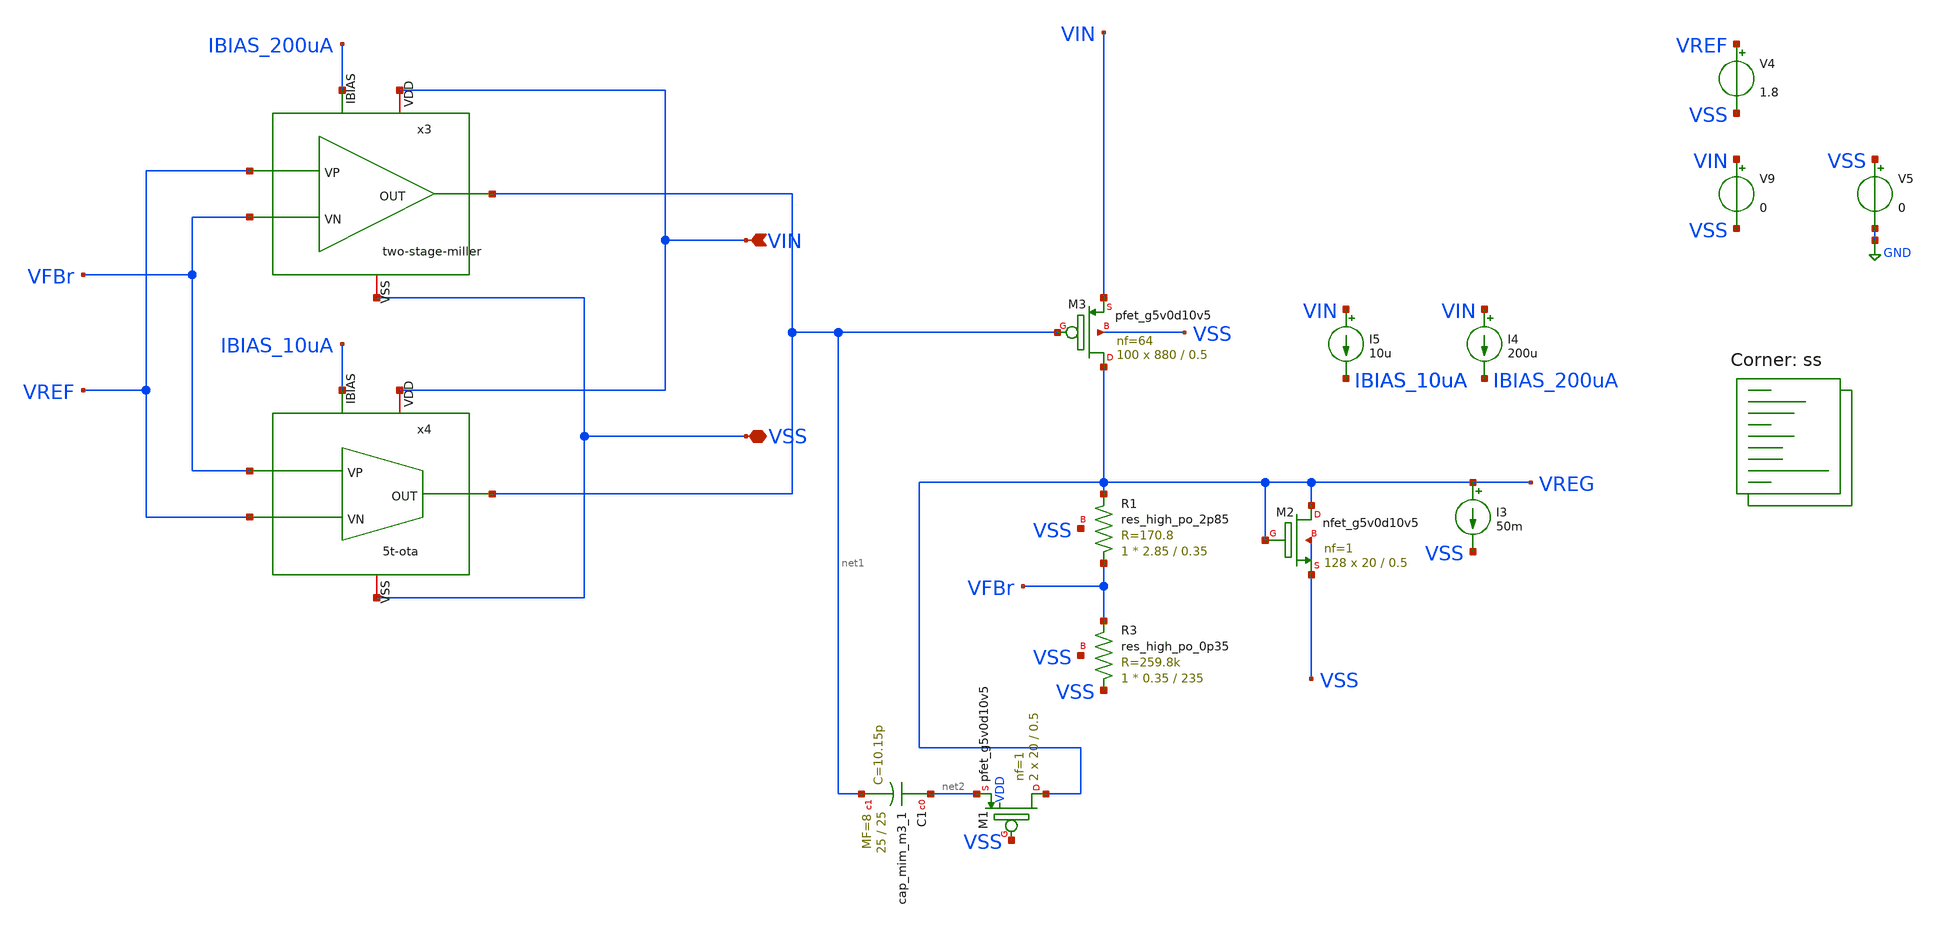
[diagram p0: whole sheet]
** sch_path: bandgap/testbench/tb_dc_dropout.sch
**.subckt tb_dc_dropout VIN VSS
*.ipin VIN
*.iopin VSS
XR3 VSS VFBr VSS sky130_fd_pr__res_high_po_0p35 L=235 mult=1 m=1
XR1 VFBr VREG VSS sky130_fd_pr__res_high_po_2p85 L=0.35 mult=1 m=1
x3 VIN net1 VREF VFBr IBIAS_200uA VSS two-stage-miller
x4 VIN net1 IBIAS_10uA VREF VFBr VSS 5t-ota
I4 VIN IBIAS_200uA 200u
I3 VREG VSS 50m
V4 VREF VSS 1.8
V5 VSS GND 0
V9 VIN VSS 0
I5 VIN IBIAS_10uA 10u
XM2 VREG VREG VSS VSS sky130_fd_pr__nfet_g5v0d10v5 L=0.5 W=20 nf=1 ad='int((nf+1)/2) * W/nf * 0.29' as='int((nf+2)/2) * W/nf * 0.29'
+ pd='2*int((nf+1)/2) * (W/nf + 0.29)' ps='2*int((nf+2)/2) * (W/nf + 0.29)' nrd='0.29 / W' nrs='0.29 / W'
+ sa=0 sb=0 sd=0 mult=128 m=128
XC1 net2 net1 sky130_fd_pr__cap_mim_m3_1 W=25 L=25 MF=8 m=8
XM1 VREG VSS net2 VDD sky130_fd_pr__pfet_g5v0d10v5 L=0.5 W=20 nf=1 ad='int((nf+1)/2) * W/nf * 0.29' as='int((nf+2)/2) * W/nf * 0.29'
+ pd='2*int((nf+1)/2) * (W/nf + 0.29)' ps='2*int((nf+2)/2) * (W/nf + 0.29)' nrd='0.29 / W' nrs='0.29 / W'
+ sa=0 sb=0 sd=0 mult=2 m=2
XM3 VREG net1 VIN VSS sky130_fd_pr__pfet_g5v0d10v5 L=0.5 W=880 nf=64 ad='int((nf+1)/2) * W/nf * 0.29'
+ as='int((nf+2)/2) * W/nf * 0.29' pd='2*int((nf+1)/2) * (W/nf + 0.29)' ps='2*int((nf+2)/2) * (W/nf + 0.29)'
+ nrd='0.29 / W' nrs='0.29 / W' sa=0 sb=0 sd=0 mult=100 m=100
**** begin user architecture code


.control
DC V9 0 5 0.01

* Nominal output voltage (from regulation region)
let Vout_nom = 0.5
let Vout_95  = 0.95*Vout_nom

* Find Vin where Vout crosses 95%
meas dc Vin_do find v(vin) when v(vreg)=Vout_95

* Measure Vout at that Vin (for completeness)
meas dc Vout_do find v(vreg) when v(vreg)=Vout_95

* Compute dropout voltage
let Vdo = Vin_do - Vout_do
print vdo
plot VIN VREG
.endc


.lib $::SKYWATER_MODELS/sky130.lib.spice ss
**** end user architecture code
**.ends

* expanding   symbol:  icdec-biomedical-pmic/xschem/error-amplifier/schematics/two-stage-miller.sym
*+ # of pins=6
** sym_path: xschem/error-amplifier/schematics/two-stage-miller.sym
** sch_path: xschem/error-amplifier/schematics/two-stage-miller.sch
.subckt two-stage-miller VDD OUT VP VN IBIAS VSS
*.iopin VDD
*.iopin VSS
*.ipin IBIAS
*.ipin VP
*.ipin VN
*.opin OUT
XM1 net3 net2 VDD VDD sky130_fd_pr__pfet_g5v0d10v5 L=1.25 W=75.2 nf=8 ad='int((nf+1)/2) * W/nf * 0.29'
+ as='int((nf+2)/2) * W/nf * 0.29' pd='2*int((nf+1)/2) * (W/nf + 0.29)' ps='2*int((nf+2)/2) * (W/nf + 0.29)'
+ nrd='0.29 / W' nrs='0.29 / W' sa=0 sb=0 sd=0 mult=1 m=1
XM2 net2 net2 VDD VDD sky130_fd_pr__pfet_g5v0d10v5 L=1.25 W=75.2 nf=8 ad='int((nf+1)/2) * W/nf * 0.29'
+ as='int((nf+2)/2) * W/nf * 0.29' pd='2*int((nf+1)/2) * (W/nf + 0.29)' ps='2*int((nf+2)/2) * (W/nf + 0.29)'
+ nrd='0.29 / W' nrs='0.29 / W' sa=0 sb=0 sd=0 mult=1 m=1
XM3 net3 VN net1 VSS sky130_fd_pr__nfet_g5v0d10v5 L=0.5 W=37.7 nf=8 ad='int((nf+1)/2) * W/nf * 0.29'
+ as='int((nf+2)/2) * W/nf * 0.29' pd='2*int((nf+1)/2) * (W/nf + 0.29)' ps='2*int((nf+2)/2) * (W/nf + 0.29)'
+ nrd='0.29 / W' nrs='0.29 / W' sa=0 sb=0 sd=0 mult=1 m=1
XM4 net2 VP net1 VSS sky130_fd_pr__nfet_g5v0d10v5 L=0.5 W=37.7 nf=8 ad='int((nf+1)/2) * W/nf * 0.29'
+ as='int((nf+2)/2) * W/nf * 0.29' pd='2*int((nf+1)/2) * (W/nf + 0.29)' ps='2*int((nf+2)/2) * (W/nf + 0.29)'
+ nrd='0.29 / W' nrs='0.29 / W' sa=0 sb=0 sd=0 mult=1 m=1
XM5 net1 IBIAS VSS VSS sky130_fd_pr__nfet_g5v0d10v5 L=1.25 W=60 nf=8 ad='int((nf+1)/2) * W/nf * 0.29'
+ as='int((nf+2)/2) * W/nf * 0.29' pd='2*int((nf+1)/2) * (W/nf + 0.29)' ps='2*int((nf+2)/2) * (W/nf + 0.29)'
+ nrd='0.29 / W' nrs='0.29 / W' sa=0 sb=0 sd=0 mult=1 m=1
XM6 IBIAS IBIAS VSS VSS sky130_fd_pr__nfet_g5v0d10v5 L=1.25 W=60 nf=8 ad='int((nf+1)/2) * W/nf * 0.29'
+ as='int((nf+2)/2) * W/nf * 0.29' pd='2*int((nf+1)/2) * (W/nf + 0.29)' ps='2*int((nf+2)/2) * (W/nf + 0.29)'
+ nrd='0.29 / W' nrs='0.29 / W' sa=0 sb=0 sd=0 mult=1 m=1
XM7 OUT net3 VDD VDD sky130_fd_pr__pfet_g5v0d10v5 L=1.25 W=160 nf=16 ad='int((nf+1)/2) * W/nf * 0.29'
+ as='int((nf+2)/2) * W/nf * 0.29' pd='2*int((nf+1)/2) * (W/nf + 0.29)' ps='2*int((nf+2)/2) * (W/nf + 0.29)'
+ nrd='0.29 / W' nrs='0.29 / W' sa=0 sb=0 sd=0 mult=1 m=1
XM8 OUT IBIAS VSS VSS sky130_fd_pr__nfet_g5v0d10v5 L=1.25 W=60 nf=8 ad='int((nf+1)/2) * W/nf * 0.29'
+ as='int((nf+2)/2) * W/nf * 0.29' pd='2*int((nf+1)/2) * (W/nf + 0.29)' ps='2*int((nf+2)/2) * (W/nf + 0.29)'
+ nrd='0.29 / W' nrs='0.29 / W' sa=0 sb=0 sd=0 mult=1 m=1
XC1 net4 net3 sky130_fd_pr__cap_mim_m3_1 W=25 L=25 MF=8 m=8
XM9 OUT VSS net4 VDD sky130_fd_pr__pfet_g5v0d10v5 L=0.9 W=20 nf=4 ad='int((nf+1)/2) * W/nf * 0.29' as='int((nf+2)/2) * W/nf * 0.29'
+ pd='2*int((nf+1)/2) * (W/nf + 0.29)' ps='2*int((nf+2)/2) * (W/nf + 0.29)' nrd='0.29 / W' nrs='0.29 / W'
+ sa=0 sb=0 sd=0 mult=1 m=1
.ends


* expanding   symbol:  icdec-biomedical-pmic/xschem/5t-ota/schematics/5t-ota.sym # of pins=6
** sym_path: xschem/5t-ota/schematics/5t-ota.sym
** sch_path: xschem/5t-ota/schematics/5t-ota.sch
.subckt 5t-ota VDD OUT IBIAS VN VP VSS
*.ipin VP
*.ipin VN
*.ipin IBIAS
*.iopin VDD
*.iopin VSS
*.opin OUT
XM1 net1 VP net2 VSS sky130_fd_pr__nfet_g5v0d10v5 L=0.75 W=8.5 nf=1 ad='int((nf+1)/2) * W/nf * 0.29'
+ as='int((nf+2)/2) * W/nf * 0.29' pd='2*int((nf+1)/2) * (W/nf + 0.29)' ps='2*int((nf+2)/2) * (W/nf + 0.29)'
+ nrd='0.29 / W' nrs='0.29 / W' sa=0 sb=0 sd=0 mult=1 m=1
XM2 OUT VN net2 VSS sky130_fd_pr__nfet_g5v0d10v5 L=0.75 W=8.5 nf=1 ad='int((nf+1)/2) * W/nf * 0.29' as='int((nf+2)/2) * W/nf * 0.29'
+ pd='2*int((nf+1)/2) * (W/nf + 0.29)' ps='2*int((nf+2)/2) * (W/nf + 0.29)' nrd='0.29 / W' nrs='0.29 / W'
+ sa=0 sb=0 sd=0 mult=1 m=1
XM3 net2 IBIAS VSS VSS sky130_fd_pr__nfet_g5v0d10v5 L=1.25 W=1.58 nf=1 ad='int((nf+1)/2) * W/nf * 0.29'
+ as='int((nf+2)/2) * W/nf * 0.29' pd='2*int((nf+1)/2) * (W/nf + 0.29)' ps='2*int((nf+2)/2) * (W/nf + 0.29)'
+ nrd='0.29 / W' nrs='0.29 / W' sa=0 sb=0 sd=0 mult=1 m=1
XM4 OUT net1 VDD VDD sky130_fd_pr__pfet_g5v0d10v5 L=1.25 W=4.85 nf=1 ad='int((nf+1)/2) * W/nf * 0.29'
+ as='int((nf+2)/2) * W/nf * 0.29' pd='2*int((nf+1)/2) * (W/nf + 0.29)' ps='2*int((nf+2)/2) * (W/nf + 0.29)'
+ nrd='0.29 / W' nrs='0.29 / W' sa=0 sb=0 sd=0 mult=1 m=1
XM5 net1 net1 VDD VDD sky130_fd_pr__pfet_g5v0d10v5 L=1.25 W=4.85 nf=1 ad='int((nf+1)/2) * W/nf * 0.29'
+ as='int((nf+2)/2) * W/nf * 0.29' pd='2*int((nf+1)/2) * (W/nf + 0.29)' ps='2*int((nf+2)/2) * (W/nf + 0.29)'
+ nrd='0.29 / W' nrs='0.29 / W' sa=0 sb=0 sd=0 mult=1 m=1
XM6 IBIAS IBIAS VSS VSS sky130_fd_pr__nfet_g5v0d10v5 L=1.25 W=1.58 nf=1 ad='int((nf+1)/2) * W/nf * 0.29'
+ as='int((nf+2)/2) * W/nf * 0.29' pd='2*int((nf+1)/2) * (W/nf + 0.29)' ps='2*int((nf+2)/2) * (W/nf + 0.29)'
+ nrd='0.29 / W' nrs='0.29 / W' sa=0 sb=0 sd=0 mult=1 m=1
.ends

.GLOBAL GND
.end
